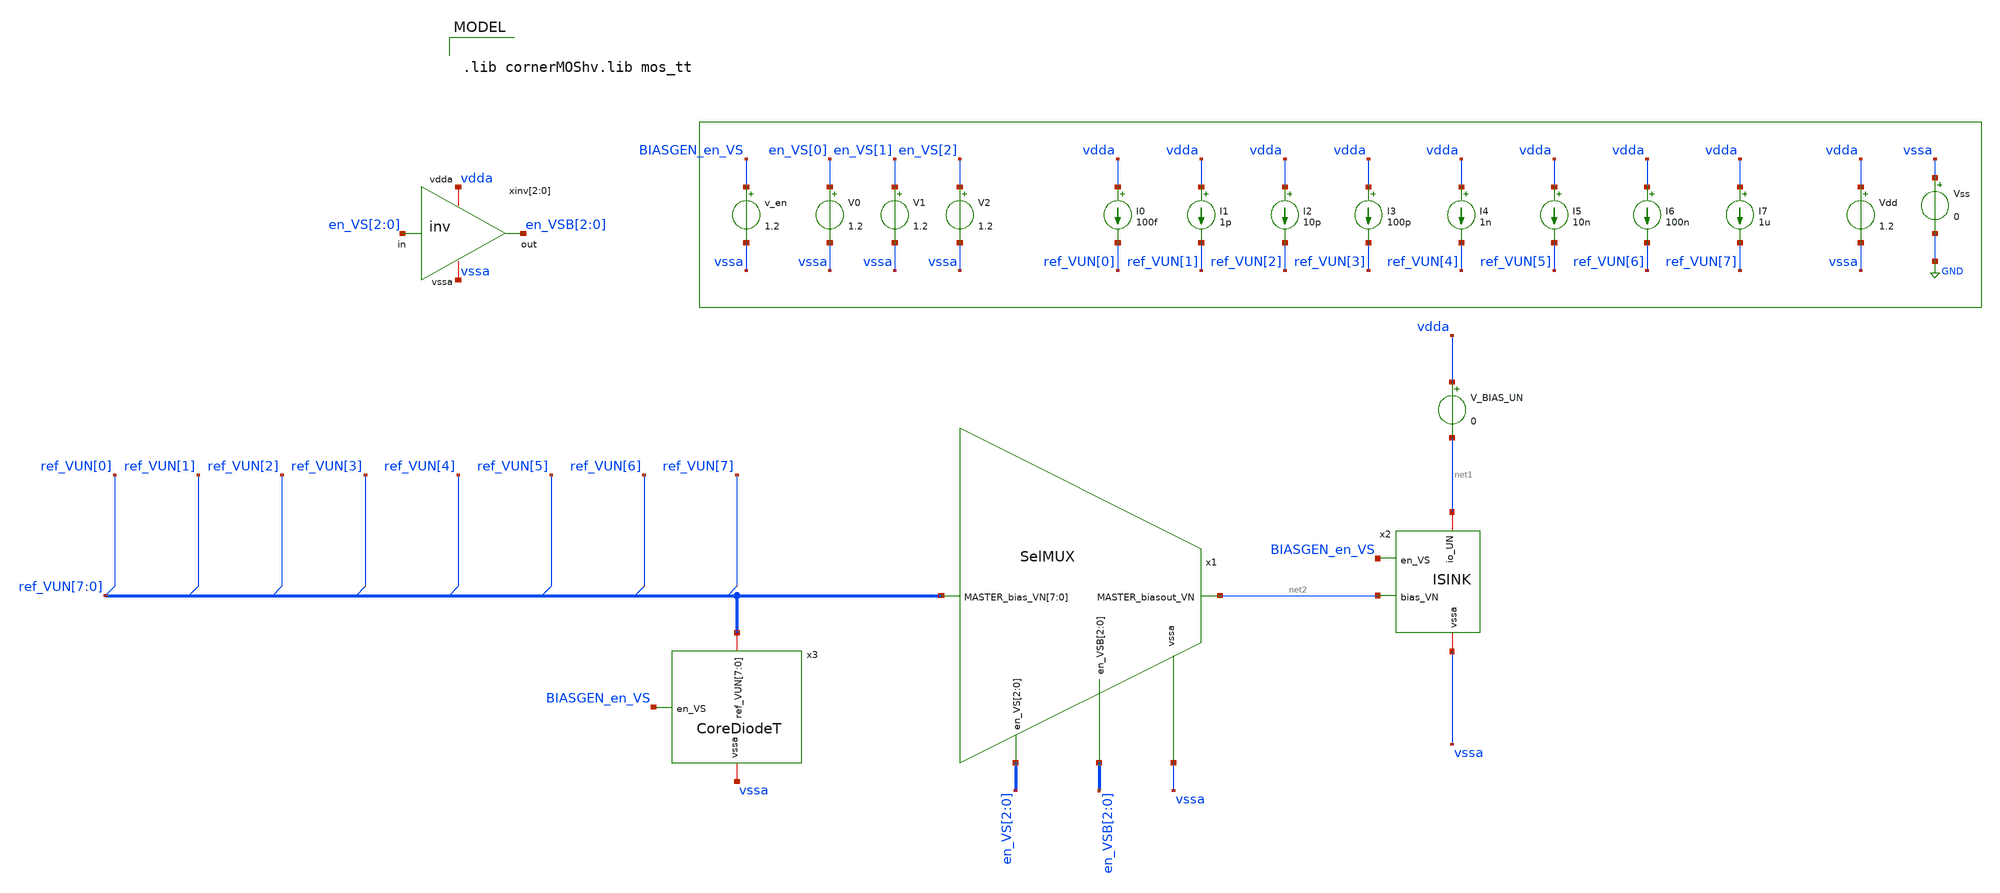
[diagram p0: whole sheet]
** sch_path: test_bench/SelMUX_dc_tb.sch
**.subckt SelMUX_dc_tb
v_en BIASGEN_en_VS vssa 1.2
Vdd vdda vssa 1.2
Vss vssa GND 0
xinv[2] vdda en_VSB[2] en_VS[2] vssa inv
xinv[1] vdda en_VSB[1] en_VS[1] vssa inv
xinv[0] vdda en_VSB[0] en_VS[0] vssa inv
V0 en_VS[0] vssa 1.2
V1 en_VS[1] vssa 1.2
V2 en_VS[2] vssa 1.2
x1 ref_VUN[7] ref_VUN[6] ref_VUN[5] ref_VUN[4] ref_VUN[3] ref_VUN[2] ref_VUN[1] ref_VUN[0] vssa
+ en_VS[2] en_VS[1] en_VS[0] en_VSB[2] en_VSB[1] en_VSB[0] net2 SelMUX
x2 net2 vssa BIASGEN_en_VS net1 ISINK
x3 ref_VUN[7] ref_VUN[6] ref_VUN[5] ref_VUN[4] ref_VUN[3] ref_VUN[2] ref_VUN[1] ref_VUN[0] vssa
+ BIASGEN_en_VS CoreDiodeT
I0 vdda ref_VUN[0] 100f
I1 vdda ref_VUN[1] 1p
I2 vdda ref_VUN[2] 10p
I3 vdda ref_VUN[3] 100p
I4 vdda ref_VUN[4] 1n
I6 vdda ref_VUN[6] 100n
I5 vdda ref_VUN[5] 10n
I7 vdda ref_VUN[7] 1u
V_BIAS_UN vdda net1 0
**** begin user architecture code

.lib cornerMOShv.lib mos_tt



.param temp=27

.options abstol=1e-15
.options gmin=1e-15
.control
save all
let digitalCommand = vector(8)
let BIAS_UN = vector(8)

let code = 0

while code < 8
    * Set the 8 bits
    alter V0 = 1.2*(code % 2)
    alter V1 = 1.2*(floor(code/2) % 2)
    alter V2 = 1.2*(floor(code/4) % 2)
    op
    let digitalCommand[code] = code
    let BIAS_UN[code] = I(V_bias_UN)
    let code = code + 1
    write SelMux_cases/SelMux_case_{$&code}.raw
end


    setplot const
    settype current BIAS_UN
    setscale digitalCommand
    plot BIAS_UN

    write SelMUC_dc_tb.raw BIAS_UN

.endc


**** end user architecture code
**.ends
.GLOBAL GND
.end
